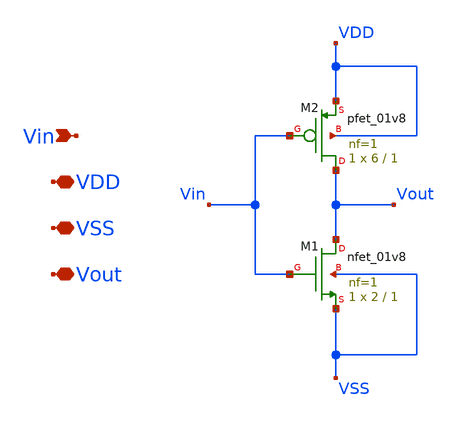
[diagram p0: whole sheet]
** sch_path: Modulo_Analogico/Lab2/inverter.sch
**.subckt inverter Vin VDD VSS Vout
*.ipin Vin
*.iopin VDD
*.iopin VSS
*.iopin Vout
XM1 Vout Vin VSS VSS sky130_fd_pr__nfet_01v8 L=1 W=2 nf=1 ad='int((1 + 1)/2) * 2 / 1 * 0.29' as='int((1 + 2)/2) * 2 / 1 * 0.29'
+ pd='2*int((1 + 1)/2) * (2 / 1 + 0.29)' ps='2*int((1 + 2)/2) * (2 / 1 + 0.29)' nrd='0.29 / 2 ' nrs='0.29 / 2 '
+ sa=0 sb=0 sd=0 mult=1 m=1
XM2 Vout Vin VDD VDD sky130_fd_pr__pfet_01v8 L=1 W=6 nf=1 ad='int((1 + 1)/2) * 6 / 1 * 0.29' as='int((1 + 2)/2) * 6 / 1 * 0.29'
+ pd='2*int((1 + 1)/2) * (6 / 1 + 0.29)' ps='2*int((1 + 2)/2) * (6 / 1 + 0.29)' nrd='0.29 / 6 ' nrs='0.29 / 6 '
+ sa=0 sb=0 sd=0 mult=1 m=1
**.ends
.end
